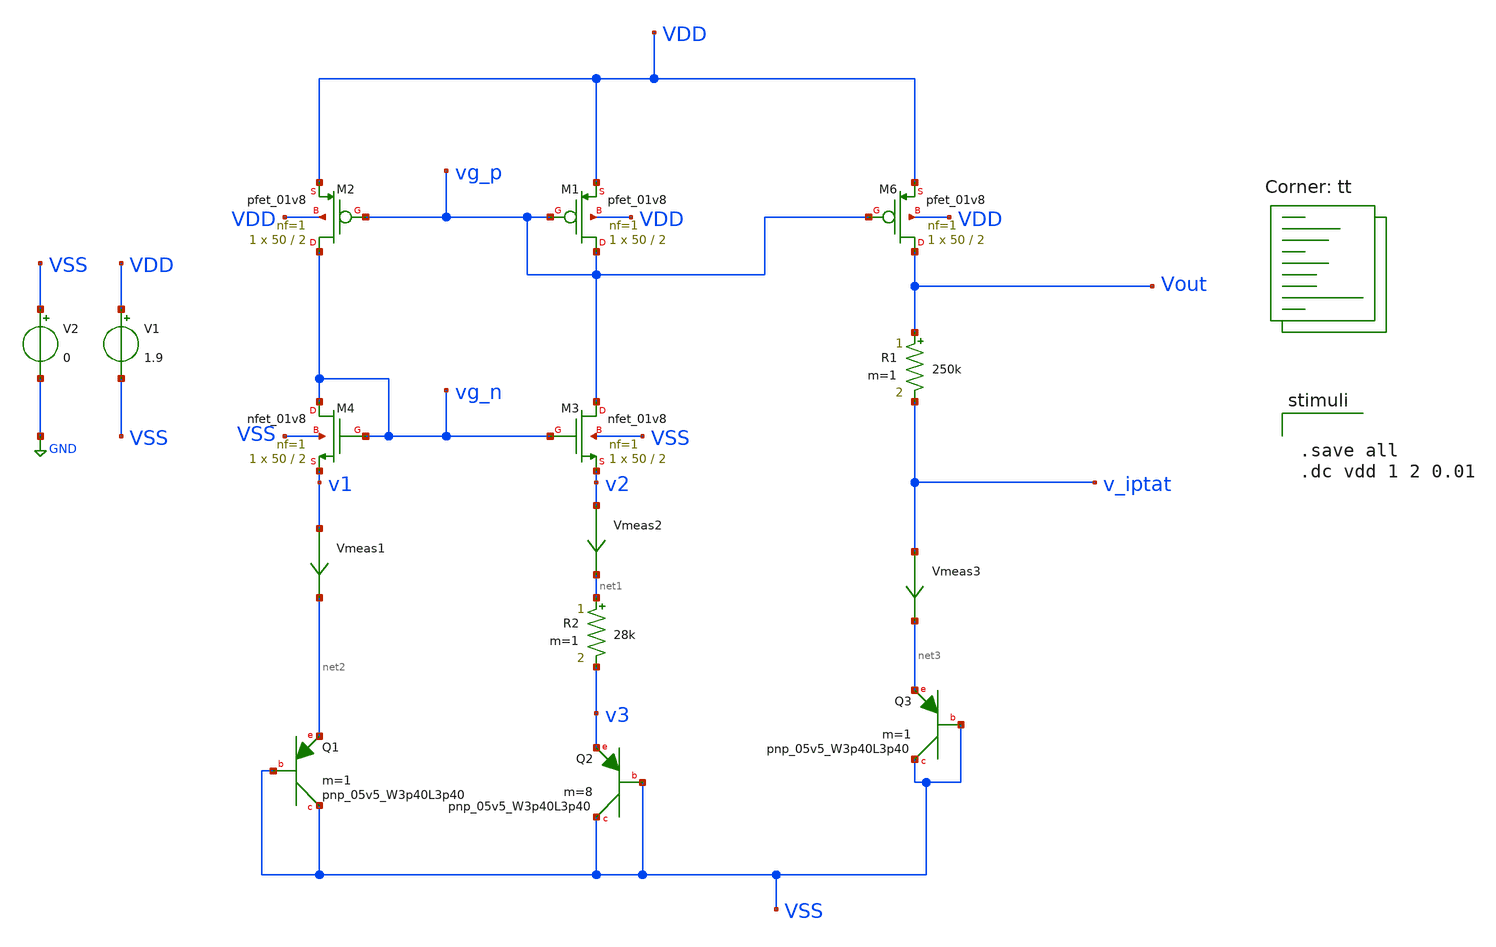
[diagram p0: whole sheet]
** sch_path: xschem/bandgap.sch
**.subckt bandgap
XM1 vg_p vg_p VDD VDD sky130_fd_pr__pfet_01v8 L=2 W=50 nf=1 ad='int((nf+1)/2) * W/nf * 0.29' as='int((nf+2)/2) * W/nf * 0.29'
+ pd='2*int((nf+1)/2) * (W/nf + 0.29)' ps='2*int((nf+2)/2) * (W/nf + 0.29)' nrd='0.29 / W' nrs='0.29 / W'
+ sa=0 sb=0 sd=0 mult=1 m=1
XM2 vg_n vg_p VDD VDD sky130_fd_pr__pfet_01v8 L=2 W=50 nf=1 ad='int((nf+1)/2) * W/nf * 0.29' as='int((nf+2)/2) * W/nf * 0.29'
+ pd='2*int((nf+1)/2) * (W/nf + 0.29)' ps='2*int((nf+2)/2) * (W/nf + 0.29)' nrd='0.29 / W' nrs='0.29 / W'
+ sa=0 sb=0 sd=0 mult=1 m=1
XM3 vg_p vg_n v2 VSS sky130_fd_pr__nfet_01v8 L=2 W=50 nf=1 ad='int((nf+1)/2) * W/nf * 0.29' as='int((nf+2)/2) * W/nf * 0.29'
+ pd='2*int((nf+1)/2) * (W/nf + 0.29)' ps='2*int((nf+2)/2) * (W/nf + 0.29)' nrd='0.29 / W' nrs='0.29 / W'
+ sa=0 sb=0 sd=0 mult=1 m=1
XM4 vg_n vg_n v1 VSS sky130_fd_pr__nfet_01v8 L=2 W=50 nf=1 ad='int((nf+1)/2) * W/nf * 0.29' as='int((nf+2)/2) * W/nf * 0.29'
+ pd='2*int((nf+1)/2) * (W/nf + 0.29)' ps='2*int((nf+2)/2) * (W/nf + 0.29)' nrd='0.29 / W' nrs='0.29 / W'
+ sa=0 sb=0 sd=0 mult=1 m=1
XQ1 VSS VSS net2 sky130_fd_pr__pnp_05v5_W3p40L3p40 m=1
V1 VDD VSS 1.9
XM6 Vout vg_p VDD VDD sky130_fd_pr__pfet_01v8 L=2 W=50 nf=1 ad='int((nf+1)/2) * W/nf * 0.29' as='int((nf+2)/2) * W/nf * 0.29'
+ pd='2*int((nf+1)/2) * (W/nf + 0.29)' ps='2*int((nf+2)/2) * (W/nf + 0.29)' nrd='0.29 / W' nrs='0.29 / W'
+ sa=0 sb=0 sd=0 mult=1 m=1
XQ3 VSS VSS net3 sky130_fd_pr__pnp_05v5_W3p40L3p40 m=1
R1 Vout v_iptat 250k m=1
XQ2 VSS VSS v3 sky130_fd_pr__pnp_05v5_W3p40L3p40 m=8
R2 net1 v3 28k m=1
V2 VSS GND 0
Vmeas1 v1 net2 0
.save i(vmeas1)
Vmeas2 v2 net1 0
.save i(vmeas2)
Vmeas3 v_iptat net3 0
.save i(vmeas3)
**** begin user architecture code


.save all
.dc vdd 1 2 0.01


.lib $::SKYWATER_MODELS/sky130.lib.spice tt
**** end user architecture code
**.ends
.GLOBAL GND
.end
